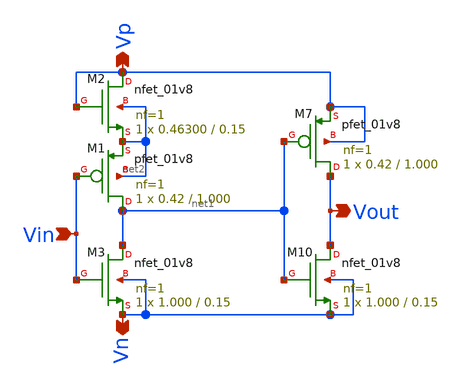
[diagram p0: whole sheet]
** sch_path: xschem/Vth_sch/Symbol/th04.sch
**.subckt th04 Vn Vp Vin Vout
*.opin Vn
*.opin Vp
*.ipin Vin
*.opin Vout
XM7 Vout net1 Vp Vp sky130_fd_pr__pfet_01v8 L=1.000 W=0.42 nf=1 ad='int((nf+1)/2) * W/nf * 0.29' as='int((nf+2)/2) * W/nf * 0.29'
+ pd='2*int((nf+1)/2) * (W/nf + 0.29)' ps='2*int((nf+2)/2) * (W/nf + 0.29)' nrd='0.29 / W' nrs='0.29 / W'
+ sa=0 sb=0 sd=0 mult=1 m=1
XM10 Vout net1 Vn Vn sky130_fd_pr__nfet_01v8 L=0.15 W=1.000 nf=1 ad='int((nf+1)/2) * W/nf * 0.29' as='int((nf+2)/2) * W/nf * 0.29'
+ pd='2*int((nf+1)/2) * (W/nf + 0.29)' ps='2*int((nf+2)/2) * (W/nf + 0.29)' nrd='0.29 / W' nrs='0.29 / W'
+ sa=0 sb=0 sd=0 mult=1 m=1
XM1 net1 Vin net2 net2 sky130_fd_pr__pfet_01v8 L=1.000 W=0.42 nf=1 ad='int((nf+1)/2) * W/nf * 0.29' as='int((nf+2)/2) * W/nf * 0.29'
+ pd='2*int((nf+1)/2) * (W/nf + 0.29)' ps='2*int((nf+2)/2) * (W/nf + 0.29)' nrd='0.29 / W' nrs='0.29 / W'
+ sa=0 sb=0 sd=0 mult=1 m=1
XM3 net1 Vin Vn Vn sky130_fd_pr__nfet_01v8 L=0.15 W=1.000 nf=1 ad='int((nf+1)/2) * W/nf * 0.29' as='int((nf+2)/2) * W/nf * 0.29'
+ pd='2*int((nf+1)/2) * (W/nf + 0.29)' ps='2*int((nf+2)/2) * (W/nf + 0.29)' nrd='0.29 / W' nrs='0.29 / W'
+ sa=0 sb=0 sd=0 mult=1 m=1
XM2 Vp Vp net2 net2 sky130_fd_pr__nfet_01v8 L=0.15 W=0.46300 nf=1 ad='int((nf+1)/2) * W/nf * 0.29' as='int((nf+2)/2) * W/nf * 0.29'
+ pd='2*int((nf+1)/2) * (W/nf + 0.29)' ps='2*int((nf+2)/2) * (W/nf + 0.29)' nrd='0.29 / W' nrs='0.29 / W'
+ sa=0 sb=0 sd=0 mult=1 m=1
**.ends
.end
